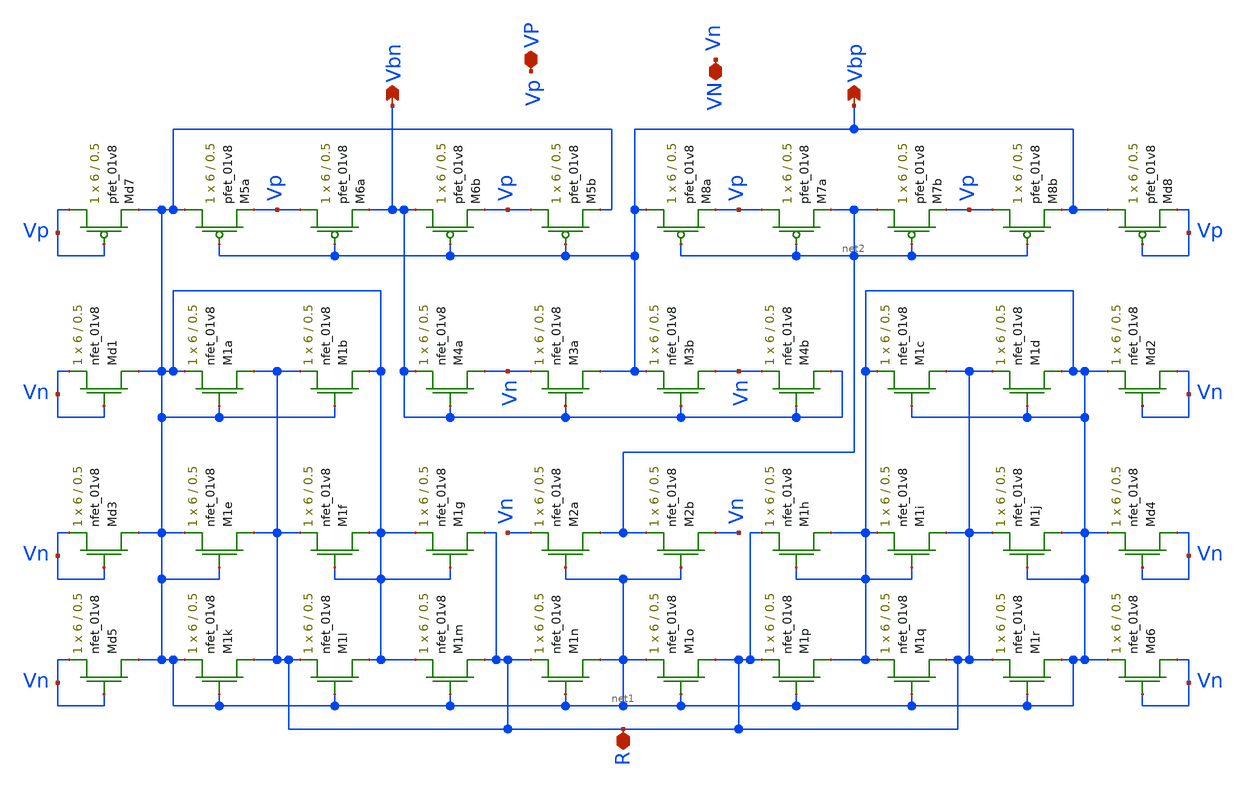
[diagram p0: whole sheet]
** sch_path: schematics/bias/current_bias_layout_driven.sch
**.subckt current_bias_layout_driven VN VP Vbn Vbp R
*.iopin VN
*.iopin VP
*.opin Vbn
*.opin Vbp
*.iopin R
XM5a net1 Vbp Vp VDD sky130_fd_pr__pfet_01v8 L=0.5 W=6 nf=1 ad='int((nf+1)/2) * W/nf * 0.29' as='int((nf+2)/2) * W/nf * 0.29'
+ pd='2*int((nf+1)/2) * (W/nf + 0.29)' ps='2*int((nf+2)/2) * (W/nf + 0.29)' nrd='0.29 / W' nrs='0.29 / W'
+ sa=0 sb=0 sd=0 mult=1 m=1
XM5b Vp Vbp net1 VDD sky130_fd_pr__pfet_01v8 L=0.5 W=6 nf=1 ad='int((nf+1)/2) * W/nf * 0.29' as='int((nf+2)/2) * W/nf * 0.29'
+ pd='2*int((nf+1)/2) * (W/nf + 0.29)' ps='2*int((nf+2)/2) * (W/nf + 0.29)' nrd='0.29 / W' nrs='0.29 / W'
+ sa=0 sb=0 sd=0 mult=1 m=1
XM1i R net1 net1 GND sky130_fd_pr__nfet_01v8 L=0.5 W=6 nf=1 ad='int((nf+1)/2) * W/nf * 0.29' as='int((nf+2)/2) * W/nf * 0.29'
+ pd='2*int((nf+1)/2) * (W/nf + 0.29)' ps='2*int((nf+2)/2) * (W/nf + 0.29)' nrd='0.29 / W' nrs='0.29 / W'
+ sa=0 sb=0 sd=0 mult=1 m=1
XM1h net1 net1 R GND sky130_fd_pr__nfet_01v8 L=0.5 W=6 nf=1 ad='int((nf+1)/2) * W/nf * 0.29' as='int((nf+2)/2) * W/nf * 0.29'
+ pd='2*int((nf+1)/2) * (W/nf + 0.29)' ps='2*int((nf+2)/2) * (W/nf + 0.29)' nrd='0.29 / W' nrs='0.29 / W'
+ sa=0 sb=0 sd=0 mult=1 m=1
XM1g R net1 net1 GND sky130_fd_pr__nfet_01v8 L=0.5 W=6 nf=1 ad='int((nf+1)/2) * W/nf * 0.29' as='int((nf+2)/2) * W/nf * 0.29'
+ pd='2*int((nf+1)/2) * (W/nf + 0.29)' ps='2*int((nf+2)/2) * (W/nf + 0.29)' nrd='0.29 / W' nrs='0.29 / W'
+ sa=0 sb=0 sd=0 mult=1 m=1
XM1f net1 net1 R GND sky130_fd_pr__nfet_01v8 L=0.5 W=6 nf=1 ad='int((nf+1)/2) * W/nf * 0.29' as='int((nf+2)/2) * W/nf * 0.29'
+ pd='2*int((nf+1)/2) * (W/nf + 0.29)' ps='2*int((nf+2)/2) * (W/nf + 0.29)' nrd='0.29 / W' nrs='0.29 / W'
+ sa=0 sb=0 sd=0 mult=1 m=1
XM1e R net1 net1 GND sky130_fd_pr__nfet_01v8 L=0.5 W=6 nf=1 ad='int((nf+1)/2) * W/nf * 0.29' as='int((nf+2)/2) * W/nf * 0.29'
+ pd='2*int((nf+1)/2) * (W/nf + 0.29)' ps='2*int((nf+2)/2) * (W/nf + 0.29)' nrd='0.29 / W' nrs='0.29 / W'
+ sa=0 sb=0 sd=0 mult=1 m=1
XM1d net1 net1 R GND sky130_fd_pr__nfet_01v8 L=0.5 W=6 nf=1 ad='int((nf+1)/2) * W/nf * 0.29' as='int((nf+2)/2) * W/nf * 0.29'
+ pd='2*int((nf+1)/2) * (W/nf + 0.29)' ps='2*int((nf+2)/2) * (W/nf + 0.29)' nrd='0.29 / W' nrs='0.29 / W'
+ sa=0 sb=0 sd=0 mult=1 m=1
XM1c R net1 net1 GND sky130_fd_pr__nfet_01v8 L=0.5 W=6 nf=1 ad='int((nf+1)/2) * W/nf * 0.29' as='int((nf+2)/2) * W/nf * 0.29'
+ pd='2*int((nf+1)/2) * (W/nf + 0.29)' ps='2*int((nf+2)/2) * (W/nf + 0.29)' nrd='0.29 / W' nrs='0.29 / W'
+ sa=0 sb=0 sd=0 mult=1 m=1
XM1b net1 net1 R GND sky130_fd_pr__nfet_01v8 L=0.5 W=6 nf=1 ad='int((nf+1)/2) * W/nf * 0.29' as='int((nf+2)/2) * W/nf * 0.29'
+ pd='2*int((nf+1)/2) * (W/nf + 0.29)' ps='2*int((nf+2)/2) * (W/nf + 0.29)' nrd='0.29 / W' nrs='0.29 / W'
+ sa=0 sb=0 sd=0 mult=1 m=1
XM1a R net1 net1 GND sky130_fd_pr__nfet_01v8 L=0.5 W=6 nf=1 ad='int((nf+1)/2) * W/nf * 0.29' as='int((nf+2)/2) * W/nf * 0.29'
+ pd='2*int((nf+1)/2) * (W/nf + 0.29)' ps='2*int((nf+2)/2) * (W/nf + 0.29)' nrd='0.29 / W' nrs='0.29 / W'
+ sa=0 sb=0 sd=0 mult=1 m=1
XM7a Vp net2 net2 VDD sky130_fd_pr__pfet_01v8 L=0.5 W=6 nf=1 ad='int((nf+1)/2) * W/nf * 0.29' as='int((nf+2)/2) * W/nf * 0.29'
+ pd='2*int((nf+1)/2) * (W/nf + 0.29)' ps='2*int((nf+2)/2) * (W/nf + 0.29)' nrd='0.29 / W' nrs='0.29 / W'
+ sa=0 sb=0 sd=0 mult=1 m=1
XM7b net2 net2 Vp VDD sky130_fd_pr__pfet_01v8 L=0.5 W=6 nf=1 ad='int((nf+1)/2) * W/nf * 0.29' as='int((nf+2)/2) * W/nf * 0.29'
+ pd='2*int((nf+1)/2) * (W/nf + 0.29)' ps='2*int((nf+2)/2) * (W/nf + 0.29)' nrd='0.29 / W' nrs='0.29 / W'
+ sa=0 sb=0 sd=0 mult=1 m=1
XM8b Vp net2 Vbp VDD sky130_fd_pr__pfet_01v8 L=0.5 W=6 nf=1 ad='int((nf+1)/2) * W/nf * 0.29' as='int((nf+2)/2) * W/nf * 0.29'
+ pd='2*int((nf+1)/2) * (W/nf + 0.29)' ps='2*int((nf+2)/2) * (W/nf + 0.29)' nrd='0.29 / W' nrs='0.29 / W'
+ sa=0 sb=0 sd=0 mult=1 m=1
XM8a Vbp net2 Vp VDD sky130_fd_pr__pfet_01v8 L=0.5 W=6 nf=1 ad='int((nf+1)/2) * W/nf * 0.29' as='int((nf+2)/2) * W/nf * 0.29'
+ pd='2*int((nf+1)/2) * (W/nf + 0.29)' ps='2*int((nf+2)/2) * (W/nf + 0.29)' nrd='0.29 / W' nrs='0.29 / W'
+ sa=0 sb=0 sd=0 mult=1 m=1
XM6b Vbn Vbp Vp VDD sky130_fd_pr__pfet_01v8 L=0.5 W=6 nf=1 ad='int((nf+1)/2) * W/nf * 0.29' as='int((nf+2)/2) * W/nf * 0.29'
+ pd='2*int((nf+1)/2) * (W/nf + 0.29)' ps='2*int((nf+2)/2) * (W/nf + 0.29)' nrd='0.29 / W' nrs='0.29 / W'
+ sa=0 sb=0 sd=0 mult=1 m=1
XM6a Vp Vbp Vbn VDD sky130_fd_pr__pfet_01v8 L=0.5 W=6 nf=1 ad='int((nf+1)/2) * W/nf * 0.29' as='int((nf+2)/2) * W/nf * 0.29'
+ pd='2*int((nf+1)/2) * (W/nf + 0.29)' ps='2*int((nf+2)/2) * (W/nf + 0.29)' nrd='0.29 / W' nrs='0.29 / W'
+ sa=0 sb=0 sd=0 mult=1 m=1
XM2a net2 net1 Vn GND sky130_fd_pr__nfet_01v8 L=0.5 W=6 nf=1 ad='int((nf+1)/2) * W/nf * 0.29' as='int((nf+2)/2) * W/nf * 0.29'
+ pd='2*int((nf+1)/2) * (W/nf + 0.29)' ps='2*int((nf+2)/2) * (W/nf + 0.29)' nrd='0.29 / W' nrs='0.29 / W'
+ sa=0 sb=0 sd=0 mult=1 m=1
XM2b Vn net1 net2 GND sky130_fd_pr__nfet_01v8 L=0.5 W=6 nf=1 ad='int((nf+1)/2) * W/nf * 0.29' as='int((nf+2)/2) * W/nf * 0.29'
+ pd='2*int((nf+1)/2) * (W/nf + 0.29)' ps='2*int((nf+2)/2) * (W/nf + 0.29)' nrd='0.29 / W' nrs='0.29 / W'
+ sa=0 sb=0 sd=0 mult=1 m=1
XM3b Vn Vbn Vbp GND sky130_fd_pr__nfet_01v8 L=0.5 W=6 nf=1 ad='int((nf+1)/2) * W/nf * 0.29' as='int((nf+2)/2) * W/nf * 0.29'
+ pd='2*int((nf+1)/2) * (W/nf + 0.29)' ps='2*int((nf+2)/2) * (W/nf + 0.29)' nrd='0.29 / W' nrs='0.29 / W'
+ sa=0 sb=0 sd=0 mult=1 m=1
XM3a Vbp Vbn Vn GND sky130_fd_pr__nfet_01v8 L=0.5 W=6 nf=1 ad='int((nf+1)/2) * W/nf * 0.29' as='int((nf+2)/2) * W/nf * 0.29'
+ pd='2*int((nf+1)/2) * (W/nf + 0.29)' ps='2*int((nf+2)/2) * (W/nf + 0.29)' nrd='0.29 / W' nrs='0.29 / W'
+ sa=0 sb=0 sd=0 mult=1 m=1
XM4a Vn Vbn Vbn GND sky130_fd_pr__nfet_01v8 L=0.5 W=6 nf=1 ad='int((nf+1)/2) * W/nf * 0.29' as='int((nf+2)/2) * W/nf * 0.29'
+ pd='2*int((nf+1)/2) * (W/nf + 0.29)' ps='2*int((nf+2)/2) * (W/nf + 0.29)' nrd='0.29 / W' nrs='0.29 / W'
+ sa=0 sb=0 sd=0 mult=1 m=1
XM4b Vbn Vbn Vn GND sky130_fd_pr__nfet_01v8 L=0.5 W=6 nf=1 ad='int((nf+1)/2) * W/nf * 0.29' as='int((nf+2)/2) * W/nf * 0.29'
+ pd='2*int((nf+1)/2) * (W/nf + 0.29)' ps='2*int((nf+2)/2) * (W/nf + 0.29)' nrd='0.29 / W' nrs='0.29 / W'
+ sa=0 sb=0 sd=0 mult=1 m=1
XM1r net1 net1 R GND sky130_fd_pr__nfet_01v8 L=0.5 W=6 nf=1 ad='int((nf+1)/2) * W/nf * 0.29' as='int((nf+2)/2) * W/nf * 0.29'
+ pd='2*int((nf+1)/2) * (W/nf + 0.29)' ps='2*int((nf+2)/2) * (W/nf + 0.29)' nrd='0.29 / W' nrs='0.29 / W'
+ sa=0 sb=0 sd=0 mult=1 m=1
XM1q R net1 net1 GND sky130_fd_pr__nfet_01v8 L=0.5 W=6 nf=1 ad='int((nf+1)/2) * W/nf * 0.29' as='int((nf+2)/2) * W/nf * 0.29'
+ pd='2*int((nf+1)/2) * (W/nf + 0.29)' ps='2*int((nf+2)/2) * (W/nf + 0.29)' nrd='0.29 / W' nrs='0.29 / W'
+ sa=0 sb=0 sd=0 mult=1 m=1
XM1p net1 net1 R GND sky130_fd_pr__nfet_01v8 L=0.5 W=6 nf=1 ad='int((nf+1)/2) * W/nf * 0.29' as='int((nf+2)/2) * W/nf * 0.29'
+ pd='2*int((nf+1)/2) * (W/nf + 0.29)' ps='2*int((nf+2)/2) * (W/nf + 0.29)' nrd='0.29 / W' nrs='0.29 / W'
+ sa=0 sb=0 sd=0 mult=1 m=1
XM1o R net1 net1 GND sky130_fd_pr__nfet_01v8 L=0.5 W=6 nf=1 ad='int((nf+1)/2) * W/nf * 0.29' as='int((nf+2)/2) * W/nf * 0.29'
+ pd='2*int((nf+1)/2) * (W/nf + 0.29)' ps='2*int((nf+2)/2) * (W/nf + 0.29)' nrd='0.29 / W' nrs='0.29 / W'
+ sa=0 sb=0 sd=0 mult=1 m=1
XM1n net1 net1 R GND sky130_fd_pr__nfet_01v8 L=0.5 W=6 nf=1 ad='int((nf+1)/2) * W/nf * 0.29' as='int((nf+2)/2) * W/nf * 0.29'
+ pd='2*int((nf+1)/2) * (W/nf + 0.29)' ps='2*int((nf+2)/2) * (W/nf + 0.29)' nrd='0.29 / W' nrs='0.29 / W'
+ sa=0 sb=0 sd=0 mult=1 m=1
XM1m R net1 net1 GND sky130_fd_pr__nfet_01v8 L=0.5 W=6 nf=1 ad='int((nf+1)/2) * W/nf * 0.29' as='int((nf+2)/2) * W/nf * 0.29'
+ pd='2*int((nf+1)/2) * (W/nf + 0.29)' ps='2*int((nf+2)/2) * (W/nf + 0.29)' nrd='0.29 / W' nrs='0.29 / W'
+ sa=0 sb=0 sd=0 mult=1 m=1
XM1l net1 net1 R GND sky130_fd_pr__nfet_01v8 L=0.5 W=6 nf=1 ad='int((nf+1)/2) * W/nf * 0.29' as='int((nf+2)/2) * W/nf * 0.29'
+ pd='2*int((nf+1)/2) * (W/nf + 0.29)' ps='2*int((nf+2)/2) * (W/nf + 0.29)' nrd='0.29 / W' nrs='0.29 / W'
+ sa=0 sb=0 sd=0 mult=1 m=1
XM1k R net1 net1 GND sky130_fd_pr__nfet_01v8 L=0.5 W=6 nf=1 ad='int((nf+1)/2) * W/nf * 0.29' as='int((nf+2)/2) * W/nf * 0.29'
+ pd='2*int((nf+1)/2) * (W/nf + 0.29)' ps='2*int((nf+2)/2) * (W/nf + 0.29)' nrd='0.29 / W' nrs='0.29 / W'
+ sa=0 sb=0 sd=0 mult=1 m=1
XM1j net1 net1 R GND sky130_fd_pr__nfet_01v8 L=0.5 W=6 nf=1 ad='int((nf+1)/2) * W/nf * 0.29' as='int((nf+2)/2) * W/nf * 0.29'
+ pd='2*int((nf+1)/2) * (W/nf + 0.29)' ps='2*int((nf+2)/2) * (W/nf + 0.29)' nrd='0.29 / W' nrs='0.29 / W'
+ sa=0 sb=0 sd=0 mult=1 m=1
XMd1 net1 Vn Vn GND sky130_fd_pr__nfet_01v8 L=0.5 W=6 nf=1 ad='int((nf+1)/2) * W/nf * 0.29' as='int((nf+2)/2) * W/nf * 0.29'
+ pd='2*int((nf+1)/2) * (W/nf + 0.29)' ps='2*int((nf+2)/2) * (W/nf + 0.29)' nrd='0.29 / W' nrs='0.29 / W'
+ sa=0 sb=0 sd=0 mult=1 m=1
XMd2 Vn Vn net1 GND sky130_fd_pr__nfet_01v8 L=0.5 W=6 nf=1 ad='int((nf+1)/2) * W/nf * 0.29' as='int((nf+2)/2) * W/nf * 0.29'
+ pd='2*int((nf+1)/2) * (W/nf + 0.29)' ps='2*int((nf+2)/2) * (W/nf + 0.29)' nrd='0.29 / W' nrs='0.29 / W'
+ sa=0 sb=0 sd=0 mult=1 m=1
XMd3 net1 Vn Vn GND sky130_fd_pr__nfet_01v8 L=0.5 W=6 nf=1 ad='int((nf+1)/2) * W/nf * 0.29' as='int((nf+2)/2) * W/nf * 0.29'
+ pd='2*int((nf+1)/2) * (W/nf + 0.29)' ps='2*int((nf+2)/2) * (W/nf + 0.29)' nrd='0.29 / W' nrs='0.29 / W'
+ sa=0 sb=0 sd=0 mult=1 m=1
XMd4 Vn Vn net1 GND sky130_fd_pr__nfet_01v8 L=0.5 W=6 nf=1 ad='int((nf+1)/2) * W/nf * 0.29' as='int((nf+2)/2) * W/nf * 0.29'
+ pd='2*int((nf+1)/2) * (W/nf + 0.29)' ps='2*int((nf+2)/2) * (W/nf + 0.29)' nrd='0.29 / W' nrs='0.29 / W'
+ sa=0 sb=0 sd=0 mult=1 m=1
XMd5 net1 Vn Vn GND sky130_fd_pr__nfet_01v8 L=0.5 W=6 nf=1 ad='int((nf+1)/2) * W/nf * 0.29' as='int((nf+2)/2) * W/nf * 0.29'
+ pd='2*int((nf+1)/2) * (W/nf + 0.29)' ps='2*int((nf+2)/2) * (W/nf + 0.29)' nrd='0.29 / W' nrs='0.29 / W'
+ sa=0 sb=0 sd=0 mult=1 m=1
XMd6 Vn Vn net1 GND sky130_fd_pr__nfet_01v8 L=0.5 W=6 nf=1 ad='int((nf+1)/2) * W/nf * 0.29' as='int((nf+2)/2) * W/nf * 0.29'
+ pd='2*int((nf+1)/2) * (W/nf + 0.29)' ps='2*int((nf+2)/2) * (W/nf + 0.29)' nrd='0.29 / W' nrs='0.29 / W'
+ sa=0 sb=0 sd=0 mult=1 m=1
XMd7 Vp Vp net1 VDD sky130_fd_pr__pfet_01v8 L=0.5 W=6 nf=1 ad='int((nf+1)/2) * W/nf * 0.29' as='int((nf+2)/2) * W/nf * 0.29'
+ pd='2*int((nf+1)/2) * (W/nf + 0.29)' ps='2*int((nf+2)/2) * (W/nf + 0.29)' nrd='0.29 / W' nrs='0.29 / W'
+ sa=0 sb=0 sd=0 mult=1 m=1
XMd8 Vbp Vp Vp VDD sky130_fd_pr__pfet_01v8 L=0.5 W=6 nf=1 ad='int((nf+1)/2) * W/nf * 0.29' as='int((nf+2)/2) * W/nf * 0.29'
+ pd='2*int((nf+1)/2) * (W/nf + 0.29)' ps='2*int((nf+2)/2) * (W/nf + 0.29)' nrd='0.29 / W' nrs='0.29 / W'
+ sa=0 sb=0 sd=0 mult=1 m=1
**.ends
.end
